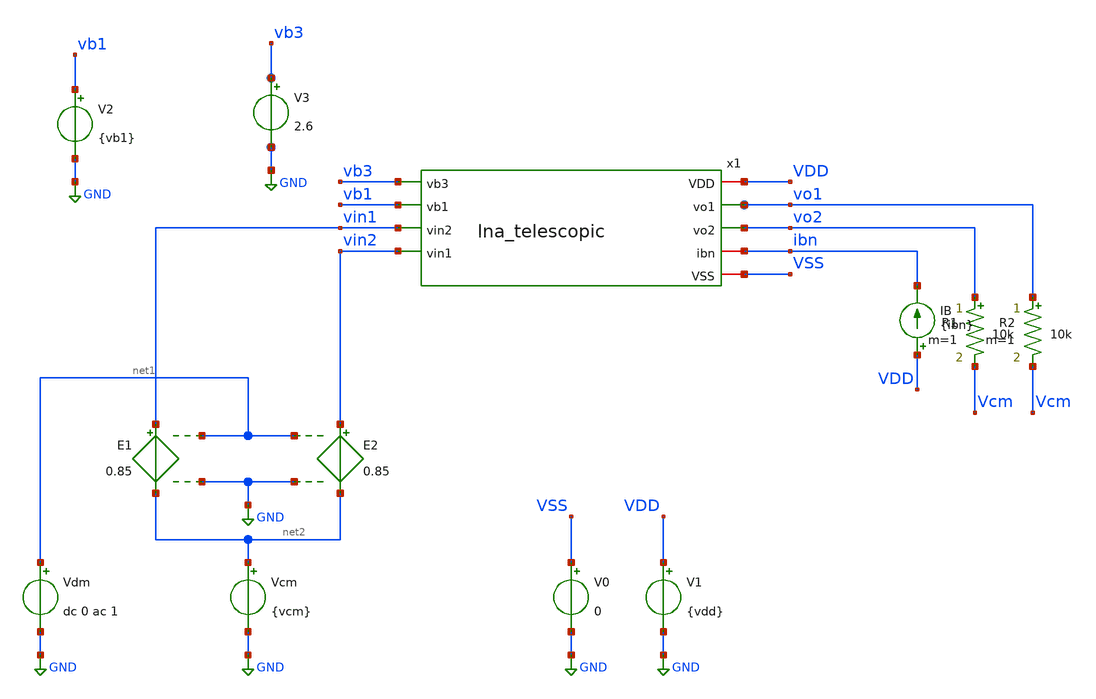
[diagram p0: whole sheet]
** sch_path: designs/lna_telescopic_tb.sch
**.subckt lna_telescopic_tb
E1 vin1 net2 net1 GND 0.85
E2 vin2 net2 net1 GND 0.85
Vdm net1 GND dc 0 ac 1
Vcm net2 GND {vcm}
V0 VSS GND 0
V1 VDD GND {vdd}
IB VDD ibn {ibn}
R1 vo2 Vcm 10k m=1
R2 vo1 Vcm 10k m=1
V2 vb1 GND {vb1}
V3 vb3 GND 2.6
x1 VDD vb3 vo1 vo2 vb1 vin1 vin2 ibn VSS lna_telescopic
**** begin user architecture code


.include /foss/pdks/gf180mcuD/libs.tech/ngspice/design.ngspice
.lib /foss/pdks/gf180mcuD/libs.tech/ngspice/sm141064.ngspice typical
.param vdd=3.3 vcm=2 ibn=5m vb1=1 vb3=1.8
.save all

.control
    save all
    op
    show all
    write lna_telescopic_tb.raw
.endc


**** end user architecture code
**.ends

* expanding   symbol:  lna_telescopic.sym # of pins=9
** sym_path: designs/libs/core_analog/lna/lna_telescopic.sym
** sch_path: designs/libs/core_analog/lna/lna_telescopic.sch
.subckt lna_telescopic VDD vb3 vo1 vo2 vb1 vin2 vin1 ibn VSS
*.ipin vb1
*.opin vo2
*.iopin VDD
*.iopin VSS
*.iopin ibn
*.ipin vin1
*.ipin vin2
*.opin vo1
*.ipin vb3
XM2b net4 vb3 VDD VDD pfet_03v3 L=0.6um W=2um nf=11 ad=0 as=0 pd=0 ps=0 nrd=0 nrs=0 sa=0 sb=0 sd=0
+ m=147
XM2a net3 vb3 VDD VDD pfet_03v3 L=0.6um W=2um nf=11 ad=0 as=0 pd=0 ps=0 nrd=0 nrs=0 sa=0 sb=0 sd=0
+ m=147
XM1a vo1 vb1 net1 VSS nfet_03v3 L=0.28um W=5um nf=10 ad=0 as=0 pd=0 ps=0 nrd=0 nrs=0 sa=0 sb=0 sd=0
+ m=19
XM0b vtail ibn VSS VSS nfet_03v3 L=0.5um W=10um nf=10 ad=0 as=0 pd=0 ps=0 nrd=0 nrs=0 sa=0 sb=0 sd=0
+ m=7
XM1b vo2 vb1 net2 VSS nfet_03v3 L=0.28um W=5um nf=10 ad=0 as=0 pd=0 ps=0 nrd=0 nrs=0 sa=0 sb=0 sd=0
+ m=19
XM0a ibn ibn VSS VSS nfet_03v3 L=0.5um W=5um nf=10 ad=0 as=0 pd=0 ps=0 nrd=0 nrs=0 sa=0 sb=0 sd=0
+ m=7
XM1 vo2 vo1 net4 VDD pfet_03v3 L=0.6um W=2um nf=11 ad=0 as=0 pd=0 ps=0 nrd=0 nrs=0 sa=0 sb=0 sd=0
+ m=92
XM2 vo1 vo1 net3 VDD pfet_03v3 L=0.6um W=2um nf=11 ad=0 as=0 pd=0 ps=0 nrd=0 nrs=0 sa=0 sb=0 sd=0
+ m=92
XM3 net1 vin1 vtail VSS nfet_03v3 L=0.28um W=5um nf=10 ad=0 as=0 pd=0 ps=0 nrd=0 nrs=0 sa=0 sb=0
+ sd=0 m=81
XM4 net2 vin2 vtail VSS nfet_03v3 L=0.28um W=5um nf=10 ad=0 as=0 pd=0 ps=0 nrd=0 nrs=0 sa=0 sb=0
+ sd=0 m=81
R1 vo1 vo1 10k m=1
R2 vo2 vo1 10k m=1
.ends

.GLOBAL GND
.end
